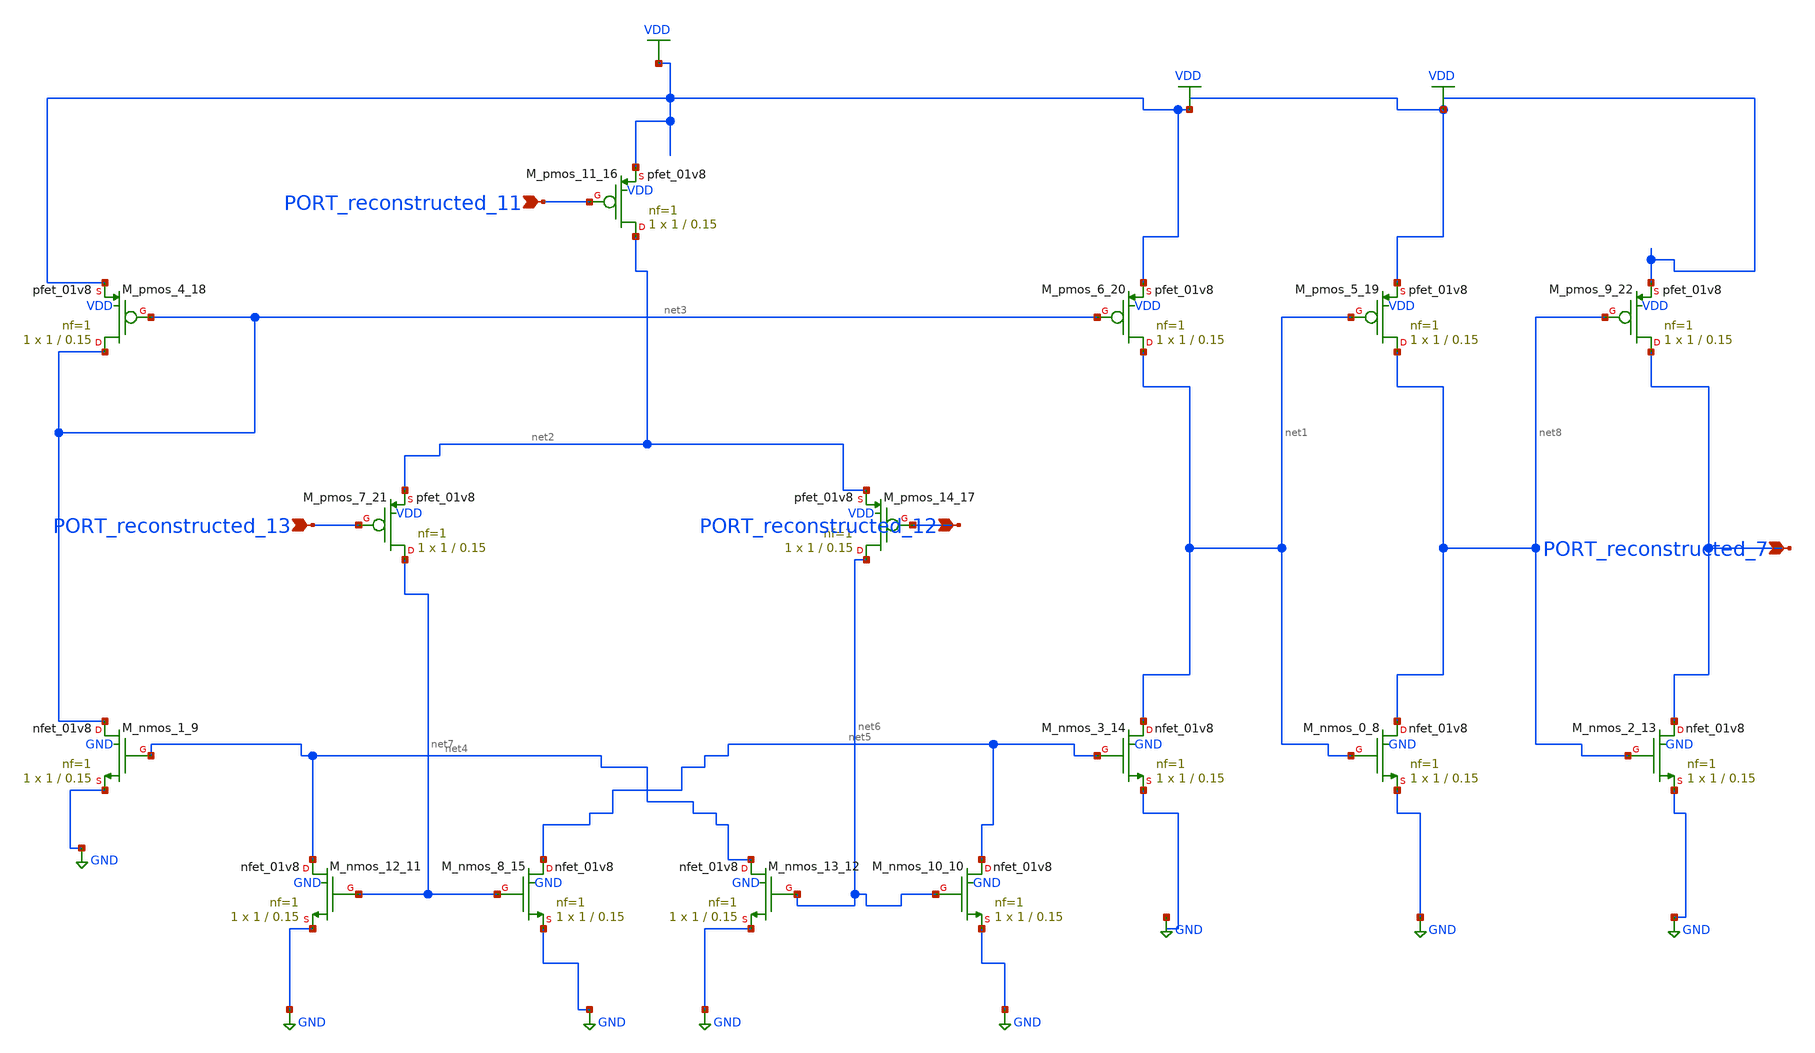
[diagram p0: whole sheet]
** sch_path: schematics/SchemGen/10_11591_eei_v12i6_5835_06_003.sch
**.subckt 10_11591_eei_v12i6_5835_06_003 PORT_reconstructed_7 PORT_reconstructed_12
*+ PORT_reconstructed_13 PORT_reconstructed_11
*.ipin PORT_reconstructed_7
*.ipin PORT_reconstructed_12
*.ipin PORT_reconstructed_13
*.ipin PORT_reconstructed_11
XM_nmos_0_8 net8 net1 GND GND sky130_fd_pr__nfet_01v8 L=0.15 W=1 nf=1 ad='int((1 + 1)/2) * 1 / 1 * 0.29'
+ as='int((1 + 2)/2) * 1 / 1 * 0.29' pd='2*int((1 + 1)/2) * (1 / 1 + 0.29)' ps='2*int((1 + 2)/2) * (1 / 1 + 0.29)'
+ nrd='0.29 / 1 ' nrs='0.29 / 1 ' sa=0 sb=0 sd=0 mult=1 m=1
XM_nmos_1_9 net3 net4 GND GND sky130_fd_pr__nfet_01v8 L=0.15 W=1 nf=1 ad='int((1 + 1)/2) * 1 / 1 * 0.29'
+ as='int((1 + 2)/2) * 1 / 1 * 0.29' pd='2*int((1 + 1)/2) * (1 / 1 + 0.29)' ps='2*int((1 + 2)/2) * (1 / 1 + 0.29)'
+ nrd='0.29 / 1 ' nrs='0.29 / 1 ' sa=0 sb=0 sd=0 mult=1 m=1
XM_nmos_10_10 net5 net6 GND GND sky130_fd_pr__nfet_01v8 L=0.15 W=1 nf=1 ad='int((1 + 1)/2) * 1 / 1 * 0.29'
+ as='int((1 + 2)/2) * 1 / 1 * 0.29' pd='2*int((1 + 1)/2) * (1 / 1 + 0.29)' ps='2*int((1 + 2)/2) * (1 / 1 + 0.29)'
+ nrd='0.29 / 1 ' nrs='0.29 / 1 ' sa=0 sb=0 sd=0 mult=1 m=1
XM_nmos_12_11 net4 net7 GND GND sky130_fd_pr__nfet_01v8 L=0.15 W=1 nf=1 ad='int((1 + 1)/2) * 1 / 1 * 0.29'
+ as='int((1 + 2)/2) * 1 / 1 * 0.29' pd='2*int((1 + 1)/2) * (1 / 1 + 0.29)' ps='2*int((1 + 2)/2) * (1 / 1 + 0.29)'
+ nrd='0.29 / 1 ' nrs='0.29 / 1 ' sa=0 sb=0 sd=0 mult=1 m=1
XM_nmos_13_12 net4 net6 GND GND sky130_fd_pr__nfet_01v8 L=0.15 W=1 nf=1 ad='int((1 + 1)/2) * 1 / 1 * 0.29'
+ as='int((1 + 2)/2) * 1 / 1 * 0.29' pd='2*int((1 + 1)/2) * (1 / 1 + 0.29)' ps='2*int((1 + 2)/2) * (1 / 1 + 0.29)'
+ nrd='0.29 / 1 ' nrs='0.29 / 1 ' sa=0 sb=0 sd=0 mult=1 m=1
XM_nmos_2_13 PORT_reconstructed_7 net8 GND GND sky130_fd_pr__nfet_01v8 L=0.15 W=1 nf=1 ad='int((1 + 1)/2) * 1 / 1 * 0.29'
+ as='int((1 + 2)/2) * 1 / 1 * 0.29' pd='2*int((1 + 1)/2) * (1 / 1 + 0.29)' ps='2*int((1 + 2)/2) * (1 / 1 + 0.29)'
+ nrd='0.29 / 1 ' nrs='0.29 / 1 ' sa=0 sb=0 sd=0 mult=1 m=1
XM_nmos_3_14 net1 net5 GND GND sky130_fd_pr__nfet_01v8 L=0.15 W=1 nf=1 ad='int((1 + 1)/2) * 1 / 1 * 0.29'
+ as='int((1 + 2)/2) * 1 / 1 * 0.29' pd='2*int((1 + 1)/2) * (1 / 1 + 0.29)' ps='2*int((1 + 2)/2) * (1 / 1 + 0.29)'
+ nrd='0.29 / 1 ' nrs='0.29 / 1 ' sa=0 sb=0 sd=0 mult=1 m=1
XM_nmos_8_15 net5 net7 GND GND sky130_fd_pr__nfet_01v8 L=0.15 W=1 nf=1 ad='int((1 + 1)/2) * 1 / 1 * 0.29'
+ as='int((1 + 2)/2) * 1 / 1 * 0.29' pd='2*int((1 + 1)/2) * (1 / 1 + 0.29)' ps='2*int((1 + 2)/2) * (1 / 1 + 0.29)'
+ nrd='0.29 / 1 ' nrs='0.29 / 1 ' sa=0 sb=0 sd=0 mult=1 m=1
XM_pmos_11_16 net2 PORT_reconstructed_11 VDD VDD sky130_fd_pr__pfet_01v8 L=0.15 W=1 nf=1 ad='int((1 + 1)/2) * 1 / 1 * 0.29'
+ as='int((1 + 2)/2) * 1 / 1 * 0.29' pd='2*int((1 + 1)/2) * (1 / 1 + 0.29)' ps='2*int((1 + 2)/2) * (1 / 1 + 0.29)'
+ nrd='0.29 / 1 ' nrs='0.29 / 1 ' sa=0 sb=0 sd=0 mult=1 m=1
XM_pmos_14_17 net6 PORT_reconstructed_12 net2 VDD sky130_fd_pr__pfet_01v8 L=0.15 W=1 nf=1 ad='int((1 + 1)/2) * 1 / 1 * 0.29'
+ as='int((1 + 2)/2) * 1 / 1 * 0.29' pd='2*int((1 + 1)/2) * (1 / 1 + 0.29)' ps='2*int((1 + 2)/2) * (1 / 1 + 0.29)'
+ nrd='0.29 / 1 ' nrs='0.29 / 1 ' sa=0 sb=0 sd=0 mult=1 m=1
XM_pmos_4_18 net3 net3 VDD VDD sky130_fd_pr__pfet_01v8 L=0.15 W=1 nf=1 ad='int((1 + 1)/2) * 1 / 1 * 0.29'
+ as='int((1 + 2)/2) * 1 / 1 * 0.29' pd='2*int((1 + 1)/2) * (1 / 1 + 0.29)' ps='2*int((1 + 2)/2) * (1 / 1 + 0.29)'
+ nrd='0.29 / 1 ' nrs='0.29 / 1 ' sa=0 sb=0 sd=0 mult=1 m=1
XM_pmos_5_19 net8 net1 VDD VDD sky130_fd_pr__pfet_01v8 L=0.15 W=1 nf=1 ad='int((1 + 1)/2) * 1 / 1 * 0.29'
+ as='int((1 + 2)/2) * 1 / 1 * 0.29' pd='2*int((1 + 1)/2) * (1 / 1 + 0.29)' ps='2*int((1 + 2)/2) * (1 / 1 + 0.29)'
+ nrd='0.29 / 1 ' nrs='0.29 / 1 ' sa=0 sb=0 sd=0 mult=1 m=1
XM_pmos_6_20 net1 net3 VDD VDD sky130_fd_pr__pfet_01v8 L=0.15 W=1 nf=1 ad='int((1 + 1)/2) * 1 / 1 * 0.29'
+ as='int((1 + 2)/2) * 1 / 1 * 0.29' pd='2*int((1 + 1)/2) * (1 / 1 + 0.29)' ps='2*int((1 + 2)/2) * (1 / 1 + 0.29)'
+ nrd='0.29 / 1 ' nrs='0.29 / 1 ' sa=0 sb=0 sd=0 mult=1 m=1
XM_pmos_7_21 net7 PORT_reconstructed_13 net2 VDD sky130_fd_pr__pfet_01v8 L=0.15 W=1 nf=1 ad='int((1 + 1)/2) * 1 / 1 * 0.29'
+ as='int((1 + 2)/2) * 1 / 1 * 0.29' pd='2*int((1 + 1)/2) * (1 / 1 + 0.29)' ps='2*int((1 + 2)/2) * (1 / 1 + 0.29)'
+ nrd='0.29 / 1 ' nrs='0.29 / 1 ' sa=0 sb=0 sd=0 mult=1 m=1
XM_pmos_9_22 PORT_reconstructed_7 net8 VDD VDD sky130_fd_pr__pfet_01v8 L=0.15 W=1 nf=1 ad='int((1 + 1)/2) * 1 / 1 * 0.29'
+ as='int((1 + 2)/2) * 1 / 1 * 0.29' pd='2*int((1 + 1)/2) * (1 / 1 + 0.29)' ps='2*int((1 + 2)/2) * (1 / 1 + 0.29)'
+ nrd='0.29 / 1 ' nrs='0.29 / 1 ' sa=0 sb=0 sd=0 mult=1 m=1
**.ends
.GLOBAL GND
.GLOBAL VDD
.end
